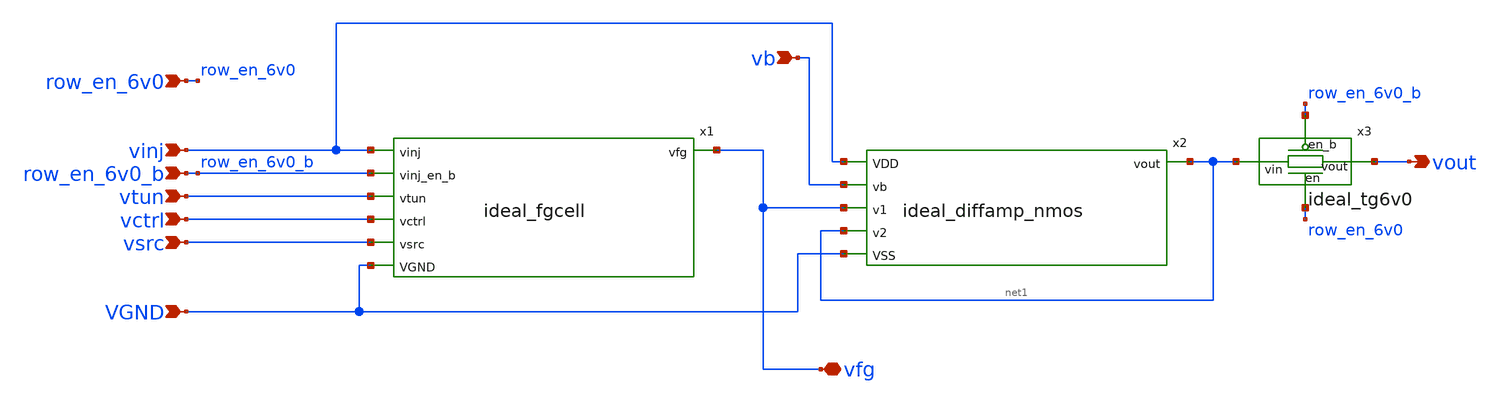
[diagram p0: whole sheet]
** sch_path: xschem/fgcell_amp.sch
**.subckt fgcell_amp vinj row_en_6v0_b vtun vctrl vsrc vb VGND vout vfg row_en_6v0
*.ipin vinj
*.ipin row_en_6v0_b
*.ipin vtun
*.ipin vctrl
*.ipin vsrc
*.ipin vb
*.ipin VGND
*.opin vout
*.iopin vfg
*.ipin row_en_6v0
x1 vinj row_en_6v0_b vtun vctrl vsrc VGND vfg ideal_fgcell
x2 net1 vfg net1 vb vinj VGND ideal_diffamp_nmos
x3 net1 vout row_en_6v0 row_en_6v0_b ideal_tg6v0
**.ends

* expanding   symbol:  ideal_fgcell.sym # of pins=7
** sym_path: xschem/ideal_fgcell.sym
** sch_path: xschem/ideal_fgcell.sch
.subckt ideal_fgcell vinj vinj_en_b vtun vctrl vsrc VGND vfg
*.ipin vctrl
*.ipin vtun
*.ipin vinj
*.ipin vinj_en_b
*.ipin vsrc
*.ipin VGND
*.opin vfg
C1 vtun vfg 1.9e-15 m=1
C2 vfg vctrl 1f m=1
S1 vinj vsrc vinj vinj_en_b sw_vinj
**** begin user architecture code


.model sw_vinj SW vt={VINJ/2} ron=14k roff=10gig


**** end user architecture code
.ends


* expanding   symbol:  ideal_diffamp_nmos.sym # of pins=6
** sym_path: xschem/ideal_diffamp_nmos.sym
** sch_path: xschem/ideal_diffamp_nmos.sch
.subckt ideal_diffamp_nmos vout v1 v2 vb VDD VSS
*.ipin v1
*.ipin v2
*.ipin VSS
*.ipin VDD
*.ipin vb
*.opin vout
E1 vout VSS v1 v2 1000
R1 VDD VSS 1meg m=1
C1 vb VSS 1f m=1
.ends


* expanding   symbol:  ideal_tg6v0.sym # of pins=4
** sym_path: xschem/ideal_tg6v0.sym
** sch_path: xschem/ideal_tg6v0.sch
.subckt ideal_tg6v0 vin vout en en_b
*.ipin vin
*.ipin en_b
*.opin vout
*.ipin en
**** begin user architecture code


.model sw_vinj SW vt=3 vh=0.1 ron=14k roff=10gig
.model sw_1v8 SW vt={1.8/2}  vh=0.1 ron=10k roff=10gig


**** end user architecture code
S1 vin vout en en_b sw_vinj
.ends

.end
